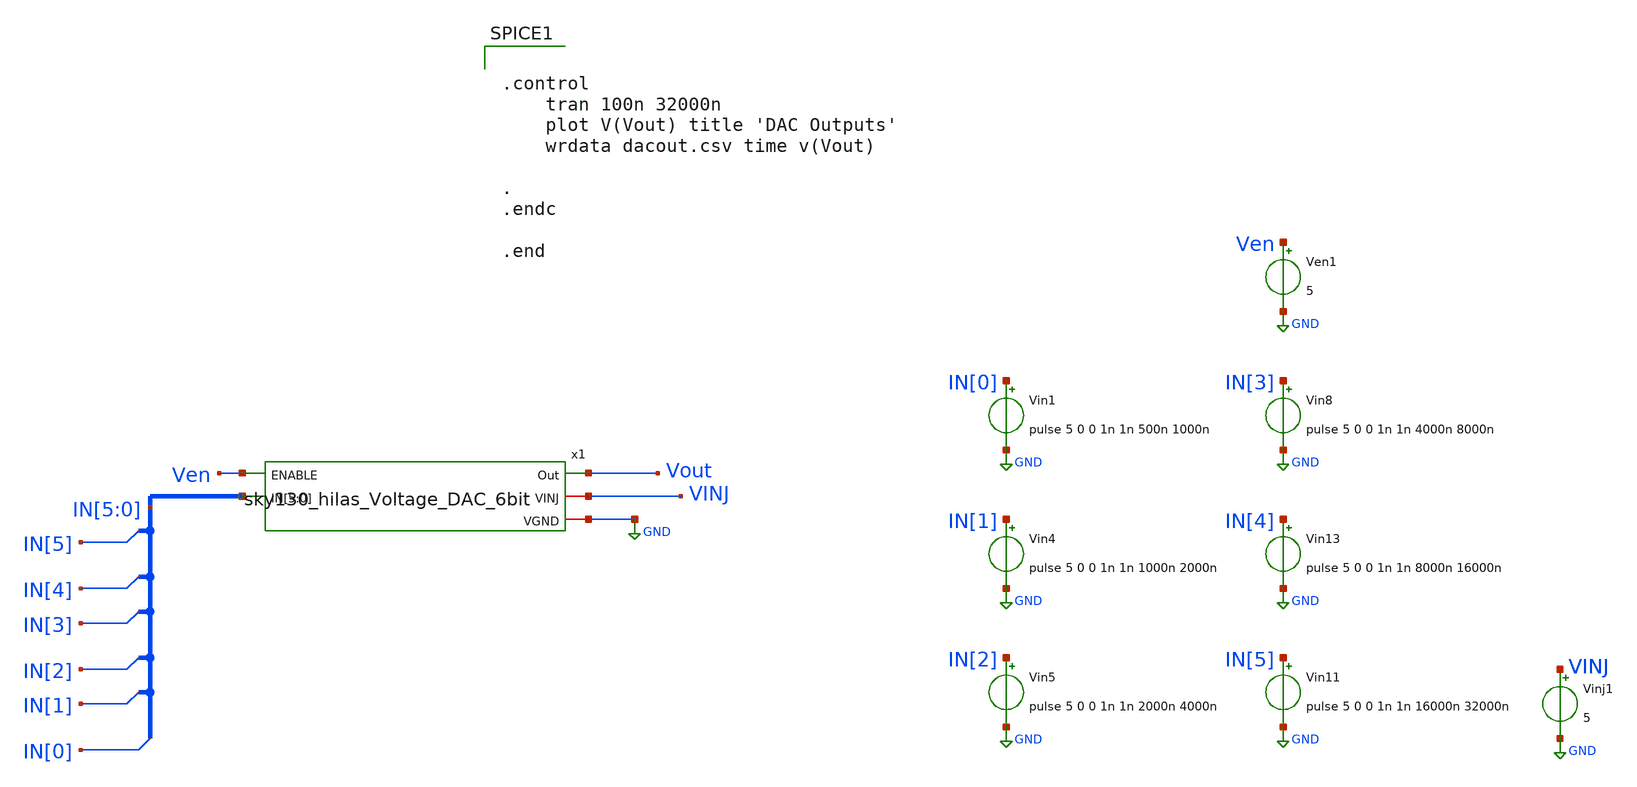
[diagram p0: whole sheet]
** sch_path: sky130_cells/RDAC/Sims/Voltage_DAC_6bit_testbench.sch
**.subckt Voltage_DAC_6bit_testbench
Vin1 IN[0] GND pulse 5 0 0 1n 1n 500n 1000n
Vin4 IN[1] GND pulse 5 0 0 1n 1n 1000n 2000n
Ven1 Ven GND 5
Vin5 IN[2] GND pulse 5 0 0 1n 1n 2000n 4000n
Vin8 IN[3] GND pulse 5 0 0 1n 1n 4000n 8000n
Vin11 IN[5] GND pulse 5 0 0 1n 1n 16000n 32000n
Vin13 IN[4] GND pulse 5 0 0 1n 1n 8000n 16000n
Vinj1 VINJ GND 5
x1 Ven IN[5] IN[4] IN[3] IN[2] IN[1] IN[0] Vout VINJ GND sky130_hilas_Voltage_DAC_6bit
**** begin user architecture code


.control
	tran 100n 32000n
	plot V(Vout) title 'DAC Outputs'
	wrdata dacout.csv time v(Vout)

.
.endc

.end


** opencircuitdesign pdks install
.lib $::SKYWATER_MODELS/sky130.lib.spice tt


**** end user architecture code
**.ends

* expanding   symbol:  sky130_cells/RDAC/Design/sky130_hilas_Voltage_DAC_6bit.sym # of pins=5
** sym_path: sky130_cells/RDAC/Design/sky130_hilas_Voltage_DAC_6bit.sym
** sch_path: sky130_cells/RDAC/Design/sky130_hilas_Voltage_DAC_6bit.sch
.subckt sky130_hilas_Voltage_DAC_6bit ENABLE IN[5] IN[4] IN[3] IN[2] IN[1] IN[0] Out VINJ VGND
*.ipin IN[5],IN[4],IN[3],IN[2],IN[1],IN[0]
*.ipin ENABLE
*.iopin VINJ
*.iopin VGND
*.opin Out
x20 VINJ IN[3] IN[2] net32 net1 net4 net3 net2 VGND sky130_hilas_VinjDecode2to4
x9 VINJ IN[3] IN[2] net33 net9 net12 net11 net10 VGND sky130_hilas_VinjDecode2to4
x14 VINJ IN[3] IN[2] net34 net17 net20 net19 net18 VGND sky130_hilas_VinjDecode2to4
x19 VINJ IN[3] IN[2] net35 net25 net28 net27 net26 VGND sky130_hilas_VinjDecode2to4
x21 VINJ IN[5] IN[4] ENABLE net35 net34 net33 net32 VGND sky130_hilas_VinjDecode2to4
x1 VINJ IN[1] IN[0] net25 Out VINJ net31 VGND sky130_hilas_CellVoltageDAC01
x2 VINJ IN[1] IN[0] net28 Out net31 net30 VGND sky130_hilas_CellVoltageDAC01
x3 VINJ IN[1] IN[0] net27 Out net30 net29 VGND sky130_hilas_CellVoltageDAC01
x4 VINJ IN[1] IN[0] net26 Out net29 net24 VGND sky130_hilas_CellVoltageDAC01
x5 VINJ IN[1] IN[0] net17 Out net24 net23 VGND sky130_hilas_CellVoltageDAC01
x6 VINJ IN[1] IN[0] net20 Out net23 net22 VGND sky130_hilas_CellVoltageDAC01
x7 VINJ IN[1] IN[0] net19 Out net22 net21 VGND sky130_hilas_CellVoltageDAC01
x8 VINJ IN[1] IN[0] net18 Out net21 net16 VGND sky130_hilas_CellVoltageDAC01
x10 VINJ IN[1] IN[0] net9 Out net16 net15 VGND sky130_hilas_CellVoltageDAC01
x11 VINJ IN[1] IN[0] net12 Out net15 net14 VGND sky130_hilas_CellVoltageDAC01
x12 VINJ IN[1] IN[0] net11 Out net14 net13 VGND sky130_hilas_CellVoltageDAC01
x13 VINJ IN[1] IN[0] net10 Out net13 net8 VGND sky130_hilas_CellVoltageDAC01
x15 VINJ IN[1] IN[0] net1 Out net8 net7 VGND sky130_hilas_CellVoltageDAC01
x16 VINJ IN[1] IN[0] net4 Out net7 net6 VGND sky130_hilas_CellVoltageDAC01
x17 VINJ IN[1] IN[0] net3 Out net6 net5 VGND sky130_hilas_CellVoltageDAC01
x18 VINJ IN[1] IN[0] net2 Out net5 VGND VGND sky130_hilas_CellVoltageDAC01
.ends


* expanding   symbol:  sky130_cells/RDAC/Design/sky130_hilas_VinjDecode2to4.sym # of pins=8
** sym_path: sky130_cells/RDAC/Design/sky130_hilas_VinjDecode2to4.sym
** sch_path: sky130_cells/RDAC/Design/sky130_hilas_VinjDecode2to4.sch
.subckt sky130_hilas_VinjDecode2to4 VINJ IN[1] IN[0] ENABLE OUTPUT00 OUTPUT01 OUTPUT10 OUTPUT11 VGND
*.ipin ENABLE
*.opin OUTPUT00
*.opin OUTPUT01
*.opin OUTPUT10
*.opin OUTPUT11
*.iopin VINJ
*.iopin VGND
*.ipin IN[1],IN[0]
x2 VINJ IN[1] VinjNOR3_2/Input2 VGND sky130_hilas_VinjInv2
x3 VINJ IN[0] VinjNOR3_1/Input1 VGND sky130_hilas_VinjInv2
x4 VINJ ENABLE VinjNOR3_3/Input3 VGND sky130_hilas_VinjInv2
x1 VINJ IN[1] IN[0] VinjNOR3_3/Input3 OUTPUT00 VGND sky130_hilas_VinjNOR3
x5 VINJ IN[1] VinjNOR3_1/Input1 VinjNOR3_3/Input3 OUTPUT01 VGND sky130_hilas_VinjNOR3
x6 VINJ VinjNOR3_2/Input2 IN[0] VinjNOR3_3/Input3 OUTPUT10 VGND sky130_hilas_VinjNOR3
x7 VINJ VinjNOR3_2/Input2 VinjNOR3_1/Input1 VinjNOR3_3/Input3 OUTPUT11 VGND sky130_hilas_VinjNOR3
.ends


* expanding   symbol:  sky130_cells/RDAC/Design/sky130_hilas_CellVoltageDAC01.sym # of pins=7
** sym_path: sky130_cells/RDAC/Design/sky130_hilas_CellVoltageDAC01.sym
** sch_path: sky130_cells/RDAC/Design/sky130_hilas_CellVoltageDAC01.sch
.subckt sky130_hilas_CellVoltageDAC01 VINJ IN[1] IN[0] ENABLE Out VREFin VREFout VGND
*.iopin VINJ
*.opin Out
*.iopin VREFout
*.ipin ENABLE
*.ipin IN[1],IN[0]
*.iopin VREFin
*.iopin VGND
x1 VINJ VREFin net1 net2 Out net3 net4 VGND VREFout sky130_hilas_dac_cell
x2 VINJ IN[1] IN[0] ENABLE net1 net2 net3 net4 VGND sky130_hilas_VinjDecode2to4
.ends


* expanding   symbol:  sky130_cells/RDAC/Design/sky130_hilas_VinjInv2.sym # of pins=4
** sym_path: sky130_cells/RDAC/Design/sky130_hilas_VinjInv2.sym
** sch_path: sky130_cells/RDAC/Design/sky130_hilas_VinjInv2.sch
.subckt sky130_hilas_VinjInv2 Vinj Input Output GND
*.ipin Input
*.opin Output
*.iopin Vinj
*.iopin GND
XM4 Output Input Vinj Vinj sky130_fd_pr__pfet_g5v0d10v5 L=0.53 W=0.42 nf=1 ad='int((nf+1)/2) * W/nf * 0.29'
+ as='int((nf+2)/2) * W/nf * 0.29' pd='2*int((nf+1)/2) * (W/nf + 0.29)' ps='2*int((nf+2)/2) * (W/nf + 0.29)'
+ nrd='0.29 / W' nrs='0.29 / W' sa=0 sb=0 sd=0 mult=1 m=1
XM3 Output Input GND GND sky130_fd_pr__nfet_g5v0d10v5 L=0.52 W=0.42 nf=1 ad='int((nf+1)/2) * W/nf * 0.29'
+ as='int((nf+2)/2) * W/nf * 0.29' pd='2*int((nf+1)/2) * (W/nf + 0.29)' ps='2*int((nf+2)/2) * (W/nf + 0.29)'
+ nrd='0.29 / W' nrs='0.29 / W' sa=0 sb=0 sd=0 mult=1 m=1
.ends


* expanding   symbol:  sky130_cells/RDAC/Design/sky130_hilas_VinjNOR3.sym # of pins=6
** sym_path: sky130_cells/RDAC/Design/sky130_hilas_VinjNOR3.sym
** sch_path: sky130_cells/RDAC/Design/sky130_hilas_VinjNOR3.sch
.subckt sky130_hilas_VinjNOR3 Vinj Input1 Input2 Input3 OUTPUT GND
*.ipin Input3
*.ipin Input1
*.ipin Input2
*.iopin Vinj
*.iopin GND
*.opin OUTPUT
XM1 OUTPUT Input3 GND GND sky130_fd_pr__nfet_g5v0d10v5 L=0.5 W=0.42 nf=1 ad='int((nf+1)/2) * W/nf * 0.29'
+ as='int((nf+2)/2) * W/nf * 0.29' pd='2*int((nf+1)/2) * (W/nf + 0.29)' ps='2*int((nf+2)/2) * (W/nf + 0.29)'
+ nrd='0.29 / W' nrs='0.29 / W' sa=0 sb=0 sd=0 mult=1 m=1
XM2 OUTPUT Input1 GND GND sky130_fd_pr__nfet_g5v0d10v5 L=0.51 W=0.43 nf=1 ad='int((nf+1)/2) * W/nf * 0.29'
+ as='int((nf+2)/2) * W/nf * 0.29' pd='2*int((nf+1)/2) * (W/nf + 0.29)' ps='2*int((nf+2)/2) * (W/nf + 0.29)'
+ nrd='0.29 / W' nrs='0.29 / W' sa=0 sb=0 sd=0 mult=1 m=1
XM3 OUTPUT Input2 GND GND sky130_fd_pr__nfet_g5v0d10v5 L=0.5 W=0.42 nf=1 ad='int((nf+1)/2) * W/nf * 0.29'
+ as='int((nf+2)/2) * W/nf * 0.29' pd='2*int((nf+1)/2) * (W/nf + 0.29)' ps='2*int((nf+2)/2) * (W/nf + 0.29)'
+ nrd='0.29 / W' nrs='0.29 / W' sa=0 sb=0 sd=0 mult=1 m=1
XM6 OUTPUT Input2 net2 Vinj sky130_fd_pr__pfet_g5v0d10v5 L=0.52 W=0.43 nf=1 ad='int((nf+1)/2) * W/nf * 0.29'
+ as='int((nf+2)/2) * W/nf * 0.29' pd='2*int((nf+1)/2) * (W/nf + 0.29)' ps='2*int((nf+2)/2) * (W/nf + 0.29)'
+ nrd='0.29 / W' nrs='0.29 / W' sa=0 sb=0 sd=0 mult=1 m=1
XM4 net2 Input1 net1 Vinj sky130_fd_pr__pfet_g5v0d10v5 L=0.52 W=0.42 nf=1 ad='int((nf+1)/2) * W/nf * 0.29'
+ as='int((nf+2)/2) * W/nf * 0.29' pd='2*int((nf+1)/2) * (W/nf + 0.29)' ps='2*int((nf+2)/2) * (W/nf + 0.29)'
+ nrd='0.29 / W' nrs='0.29 / W' sa=0 sb=0 sd=0 mult=1 m=1
XM5 net1 Input3 Vinj Vinj sky130_fd_pr__pfet_g5v0d10v5 L=0.53 W=0.42 nf=1 ad='int((nf+1)/2) * W/nf * 0.29'
+ as='int((nf+2)/2) * W/nf * 0.29' pd='2*int((nf+1)/2) * (W/nf + 0.29)' ps='2*int((nf+2)/2) * (W/nf + 0.29)'
+ nrd='0.29 / W' nrs='0.29 / W' sa=0 sb=0 sd=0 mult=1 m=1
.ends


* expanding   symbol:  sky130_cells/RDAC/Design/sky130_hilas_dac_cell.sym # of pins=9
** sym_path: sky130_cells/RDAC/Design/sky130_hilas_dac_cell.sym
** sch_path: sky130_cells/RDAC/Design/sky130_hilas_dac_cell.sch
.subckt sky130_hilas_dac_cell VDD VREFin D0 D1 Out D2 D3 GND VREFout
*.iopin VDD
*.opin Out
*.ipin D0
*.ipin D1
*.ipin D2
*.ipin D3
*.iopin GND
*.iopin VREFout
*.iopin VREFin
x1 VDD Out D0 Node[0] GND Tgate
x2 VDD Out D1 Node[1] GND Tgate
x3 VDD Out D2 Node[2] GND Tgate
x4 VDD Out D3 Node[3] GND Tgate
x5 VREFin Node[3] Node[2] Node[1] Node[0] VREFout sky130_hilas_resistor_string
.ends


* expanding   symbol:  sky130_cells/RDAC/Design/Tgate.sym # of pins=5
** sym_path: sky130_cells/RDAC/Design/Tgate.sym
** sch_path: sky130_cells/RDAC/Design/Tgate.sch
.subckt Tgate VINJ OUTPUT SELECT INPUT VGND
*.iopin VINJ
*.ipin SELECT
*.iopin INPUT
*.iopin OUTPUT
*.ipin VGND
XM5 net1 SELECT VGND VGND sky130_fd_pr__nfet_g5v0d10v5 L=0.5 W=0.42 nf=1 ad='int((1 + 1)/2) * 0.42 / 1 * 0.29'
+ as='int((1 + 2)/2) * 0.42 / 1 * 0.29' pd='2*int((1 + 1)/2) * (0.42 / 1 + 0.29)' ps='2*int((1 + 2)/2) * (0.42 / 1 + 0.29)'
+ nrd='0.29 / 0.42 ' nrs='0.29 / 0.42 ' sa=0 sb=0 sd=0 mult=1 m=1
XM1 net1 SELECT VINJ VINJ sky130_fd_pr__pfet_g5v0d10v5 L=0.5 W=0.42 nf=1 ad='int((1 + 1)/2) * 0.42 / 1 * 0.29'
+ as='int((1 + 2)/2) * 0.42 / 1 * 0.29' pd='2*int((1 + 1)/2) * (0.42 / 1 + 0.29)' ps='2*int((1 + 2)/2) * (0.42 / 1 + 0.29)'
+ nrd='0.29 / 0.42 ' nrs='0.29 / 0.42 ' sa=0 sb=0 sd=0 mult=1 m=1
XM2 INPUT net1 OUTPUT VINJ sky130_fd_pr__pfet_g5v0d10v5 L=0.5 W=0.42 nf=1 ad='int((1 + 1)/2) * 0.42 / 1 * 0.29'
+ as='int((1 + 2)/2) * 0.42 / 1 * 0.29' pd='2*int((1 + 1)/2) * (0.42 / 1 + 0.29)' ps='2*int((1 + 2)/2) * (0.42 / 1 + 0.29)'
+ nrd='0.29 / 0.42 ' nrs='0.29 / 0.42 ' sa=0 sb=0 sd=0 mult=1 m=1
XM3 OUTPUT SELECT INPUT VGND sky130_fd_pr__nfet_g5v0d10v5 L=0.5 W=0.42 nf=1 ad='int((1 + 1)/2) * 0.42 / 1 * 0.29'
+ as='int((1 + 2)/2) * 0.42 / 1 * 0.29' pd='2*int((1 + 1)/2) * (0.42 / 1 + 0.29)' ps='2*int((1 + 2)/2) * (0.42 / 1 + 0.29)'
+ nrd='0.29 / 0.42 ' nrs='0.29 / 0.42 ' sa=0 sb=0 sd=0 mult=1 m=1
.ends


* expanding   symbol:  sky130_cells/RDAC/Design/sky130_hilas_resistor_string.sym # of pins=3
** sym_path: sky130_cells/RDAC/Design/sky130_hilas_resistor_string.sym
** sch_path: sky130_cells/RDAC/Design/sky130_hilas_resistor_string.sch
.subckt sky130_hilas_resistor_string VREFin Node[3] Node[2] Node[1] Node[0] VREFout
*.iopin VREFout
*.iopin VREFin
*.opin Node[3],Node[2],Node[1],Node[0]
XR1 Node[0] VREFin sky130_fd_pr__res_generic_po W=0.33 L=10.19 m=1
XR2 net1 Node[0] sky130_fd_pr__res_generic_po W=0.33 L=10.19 m=1
XR3 Node[1] net1 sky130_fd_pr__res_generic_po W=0.33 L=10.19 m=1
XR4 net2 Node[1] sky130_fd_pr__res_generic_po W=0.33 L=10.19 m=1
XR5 Node[2] net2 sky130_fd_pr__res_generic_po W=0.33 L=10.19 m=1
XR6 net3 Node[2] sky130_fd_pr__res_generic_po W=0.33 L=10.19 m=1
XR7 Node[3] net3 sky130_fd_pr__res_generic_po W=0.33 L=10.19 m=1
XR8 VREFout Node[3] sky130_fd_pr__res_generic_po W=0.33 L=10.19 m=1
.ends

.GLOBAL GND
.end
